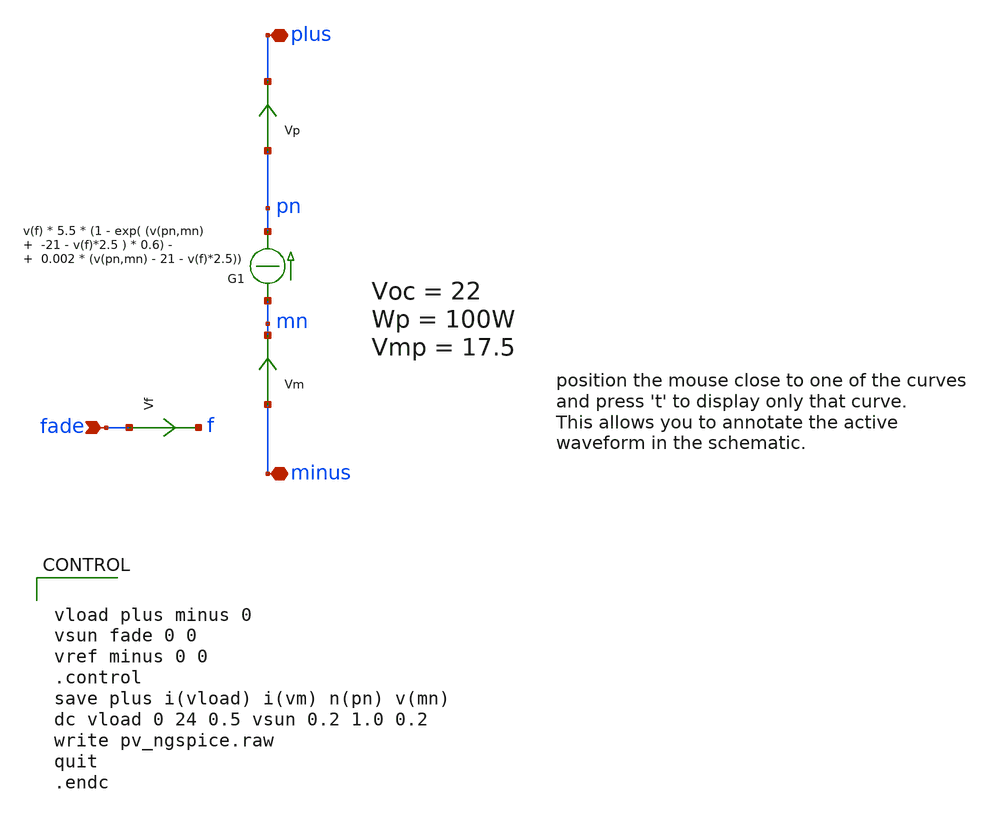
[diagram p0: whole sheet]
** sch_path: xschem_library/ngspice/pv_ngspice.sch
**.subckt pv_ngspice plus minus fade
*.iopin plus
*.iopin minus
*.ipin fade
Vm minus mn 0
.save i(vm)
G1 mn pn CUR=' v(f) * 5.5 * (1 - exp( (v(pn,mn) -21 - v(f)*2.5 ) * 0.6) - 0.002 * (v(pn,mn) - 21 - v(f)*2.5)) '
Vf fade f 0
.save i(vf)
Vp pn plus 0
.save i(vp)
**** begin user architecture code


vload plus minus 0
vsun fade 0 0
vref minus 0 0
.control
save plus i(vload) i(vm) n(pn) v(mn)
dc vload 0 24 0.5 vsun 0.2 1.0 0.2
write pv_ngspice.raw
quit
.endc


**** end user architecture code
**.ends
.end
